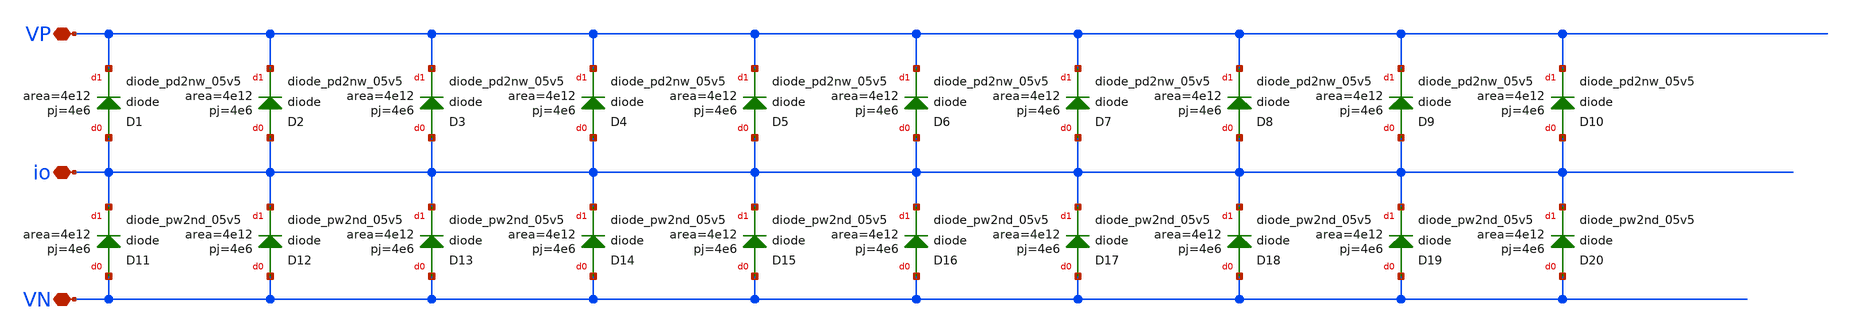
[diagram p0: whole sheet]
** sch_path: xschem/esd/esd_diodes.sch
**.subckt esd_diodes VP io VN
*.iopin VP
*.iopin io
*.iopin VN
XD1 io VP sky130_fd_pr__diode_pd2nw_05v5 area=4e12 pj=4e6
XD11 VN io sky130_fd_pr__diode_pw2nd_05v5 area=4e12 pj=4e6
XD12 VN io sky130_fd_pr__diode_pw2nd_05v5 area=4e12 pj=4e6
XD13 VN io sky130_fd_pr__diode_pw2nd_05v5 area=4e12 pj=4e6
XD14 VN io sky130_fd_pr__diode_pw2nd_05v5 area=4e12 pj=4e6
XD15 VN io sky130_fd_pr__diode_pw2nd_05v5 area=4e12 pj=4e6
XD16 VN io sky130_fd_pr__diode_pw2nd_05v5 area=4e12 pj=4e6
XD17 VN io sky130_fd_pr__diode_pw2nd_05v5 area=4e12 pj=4e6
XD18 VN io sky130_fd_pr__diode_pw2nd_05v5 area=4e12 pj=4e6
XD19 VN io sky130_fd_pr__diode_pw2nd_05v5 area=4e12 pj=4e6
XD20 VN io sky130_fd_pr__diode_pw2nd_05v5 area=4e12 pj=4e6
XD2 io VP sky130_fd_pr__diode_pd2nw_05v5 area=4e12 pj=4e6
XD3 io VP sky130_fd_pr__diode_pd2nw_05v5 area=4e12 pj=4e6
XD4 io VP sky130_fd_pr__diode_pd2nw_05v5 area=4e12 pj=4e6
XD5 io VP sky130_fd_pr__diode_pd2nw_05v5 area=4e12 pj=4e6
XD6 io VP sky130_fd_pr__diode_pd2nw_05v5 area=4e12 pj=4e6
XD7 io VP sky130_fd_pr__diode_pd2nw_05v5 area=4e12 pj=4e6
XD8 io VP sky130_fd_pr__diode_pd2nw_05v5 area=4e12 pj=4e6
XD9 io VP sky130_fd_pr__diode_pd2nw_05v5 area=4e12 pj=4e6
XD10 io VP sky130_fd_pr__diode_pd2nw_05v5 area=4e12 pj=4e6
**.ends
.end
